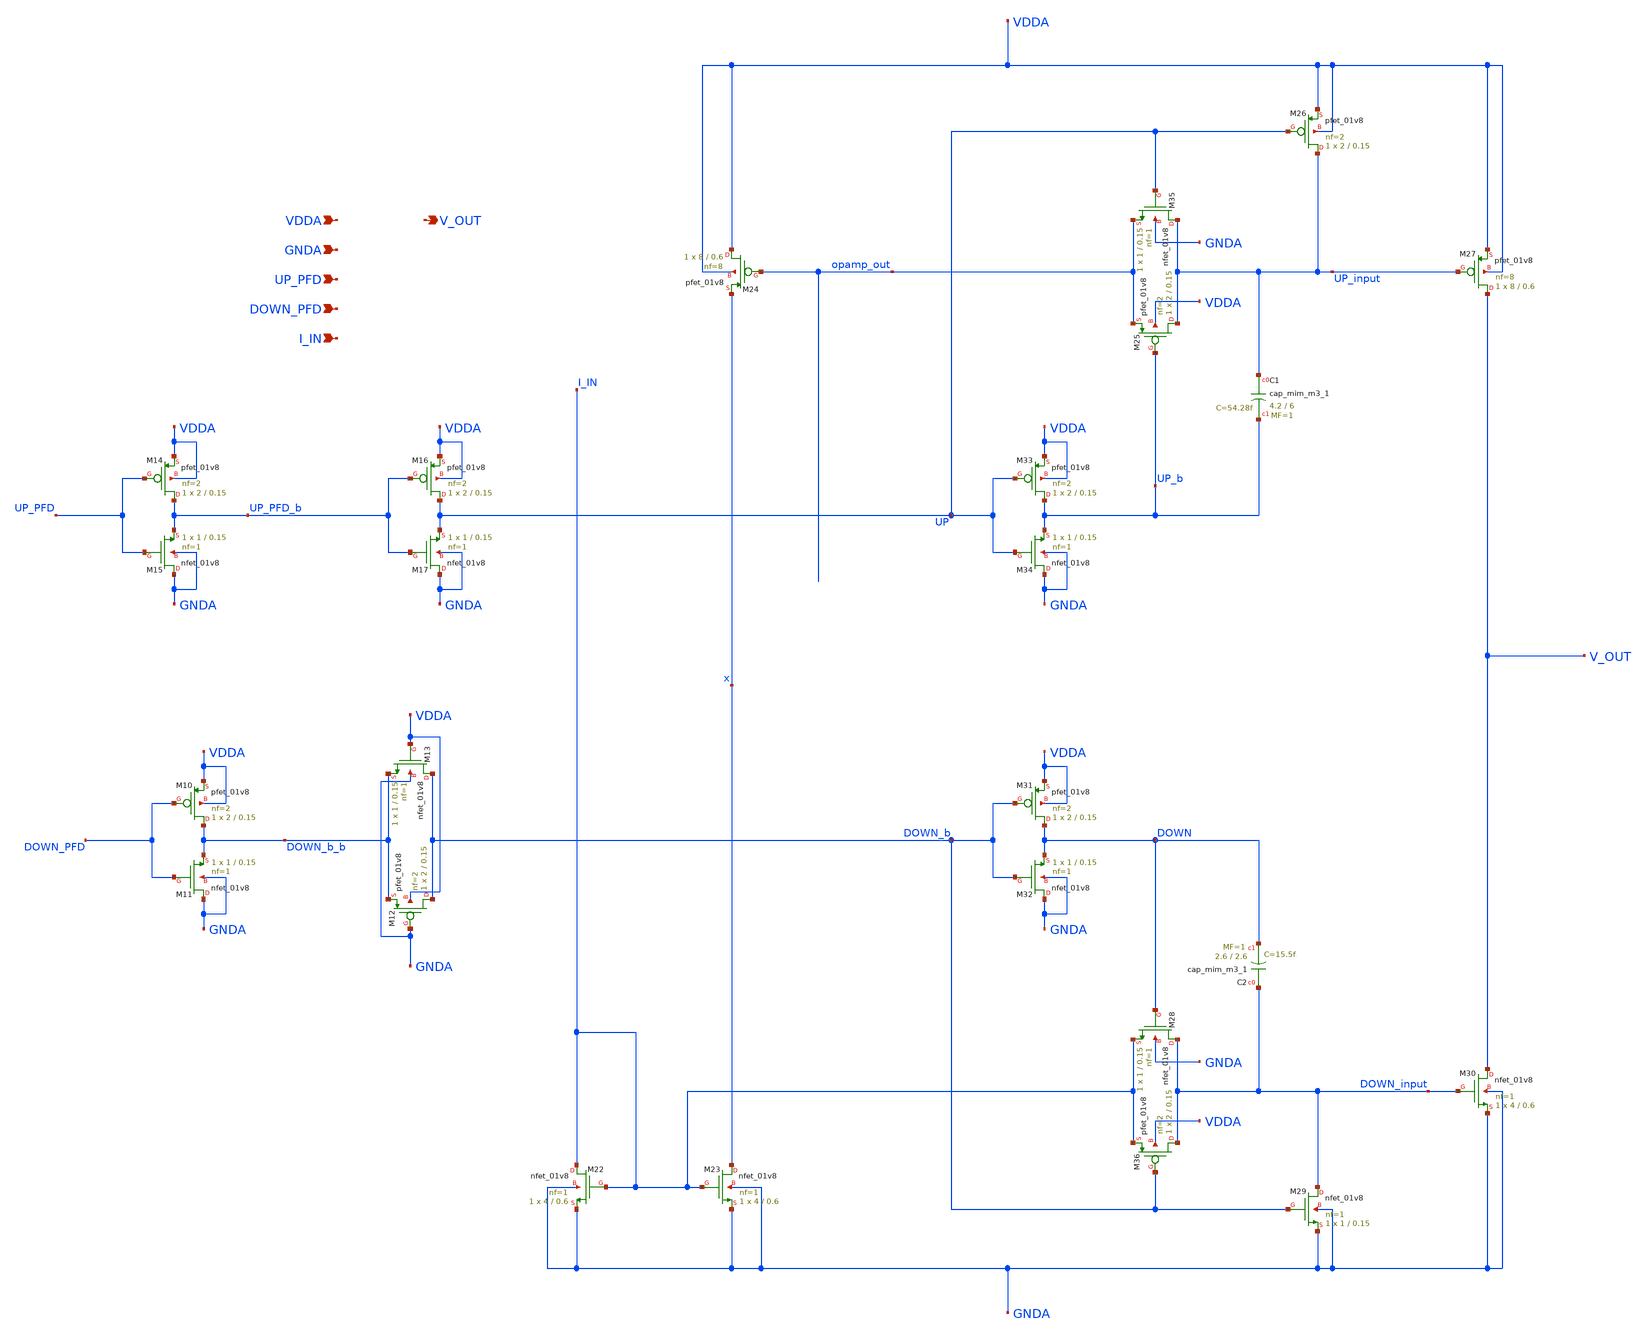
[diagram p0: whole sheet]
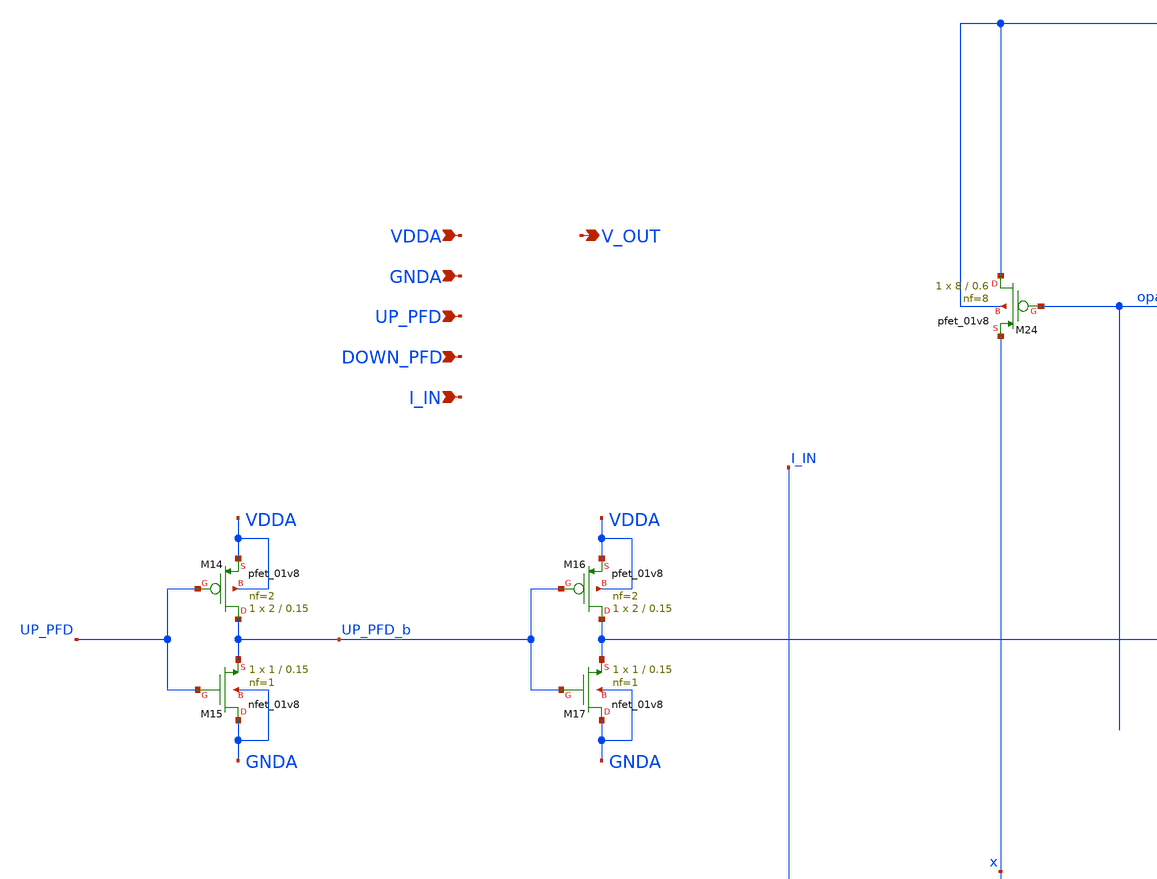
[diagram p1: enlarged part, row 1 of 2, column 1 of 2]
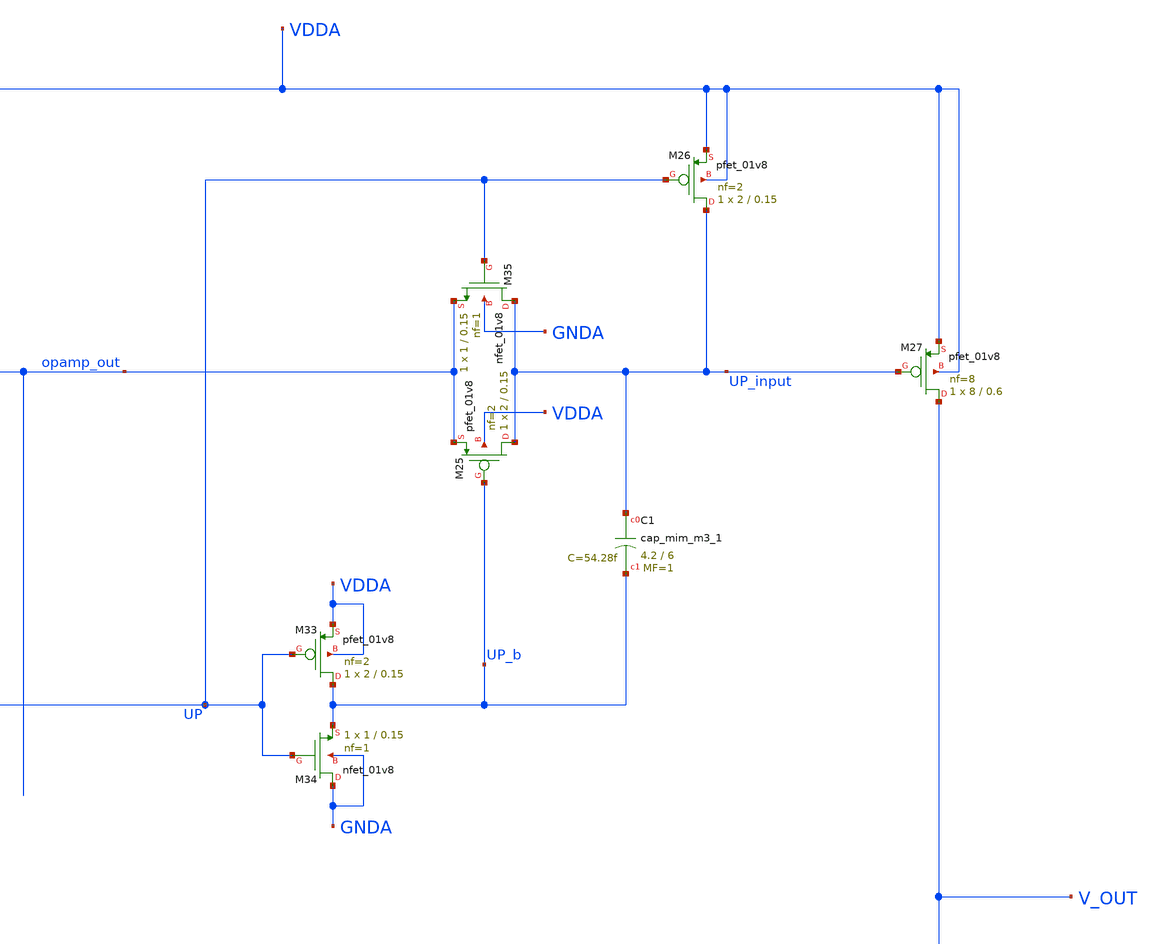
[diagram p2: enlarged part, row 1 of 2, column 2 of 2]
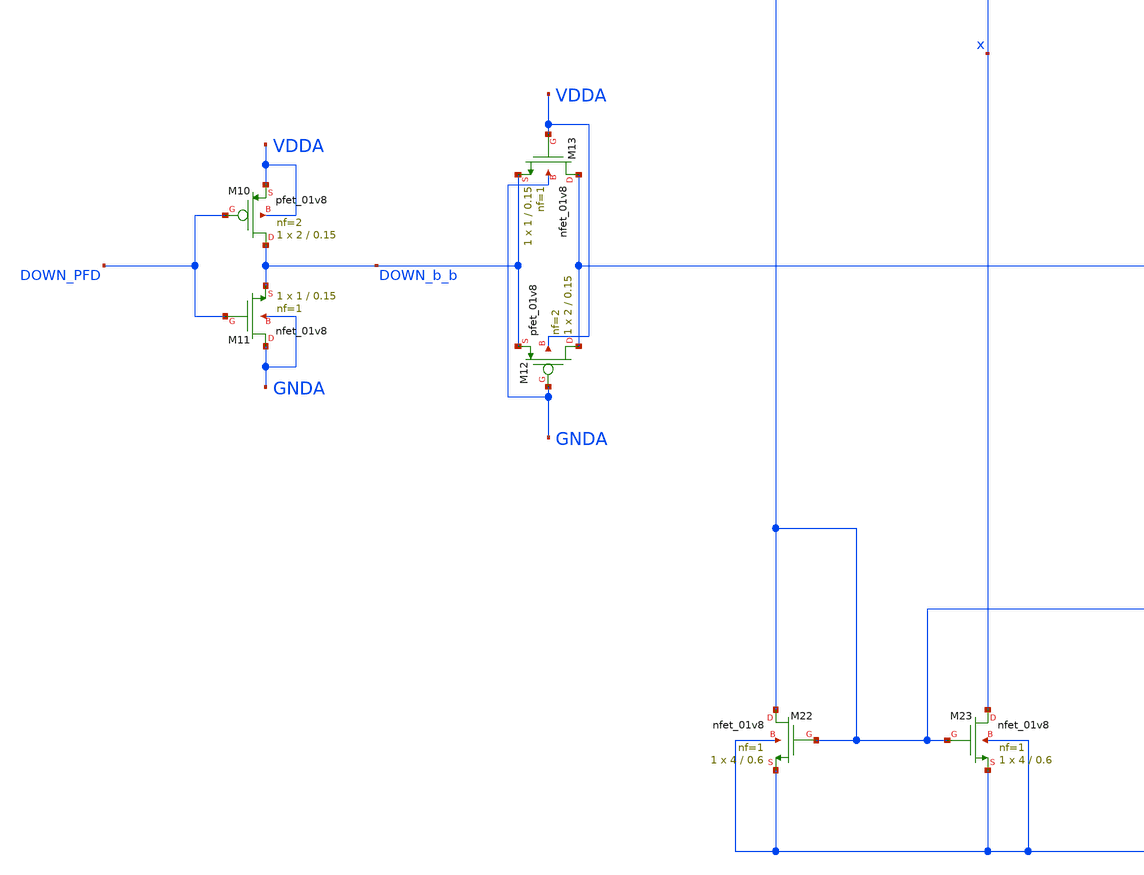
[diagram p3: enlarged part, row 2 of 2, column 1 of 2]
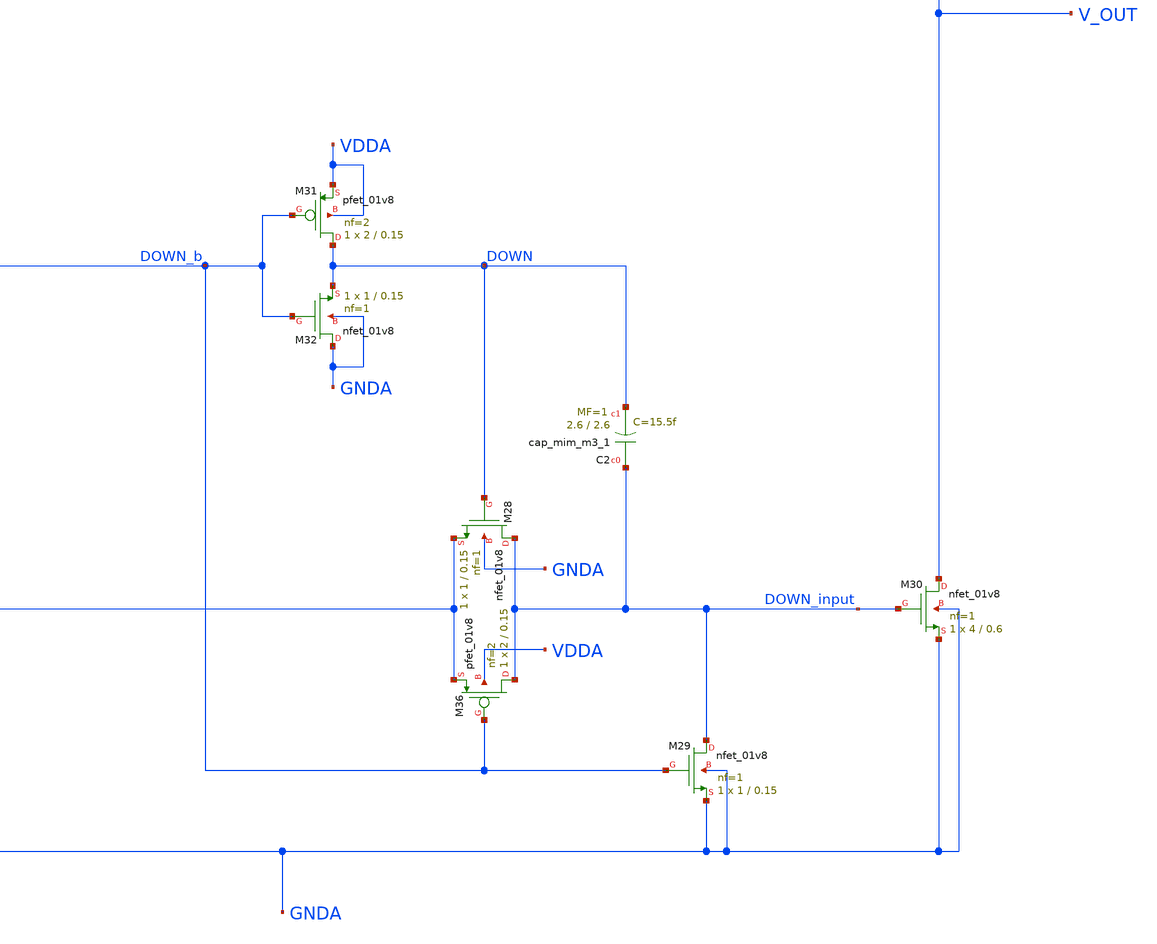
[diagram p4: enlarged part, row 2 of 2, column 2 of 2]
** sch_path: projects/pll/charge_pump/xschem_ngspice/charge_pump_xschem.sch
**.subckt charge_pump_xschem VDDA V_OUT GNDA UP_PFD DOWN_PFD I_IN
*.ipin VDDA
*.opin V_OUT
*.ipin GNDA
*.ipin UP_PFD
*.ipin DOWN_PFD
*.ipin I_IN
XM12 DOWN_b GNDA DOWN_b_b VDDA sky130_fd_pr__pfet_01v8 L=0.15 W=2 nf=2 ad='int((nf+1)/2) * W/nf * 0.29'
+ as='int((nf+2)/2) * W/nf * 0.29' pd='2*int((nf+1)/2) * (W/nf + 0.29)' ps='2*int((nf+2)/2) * (W/nf + 0.29)'
+ nrd='0.29 / W' nrs='0.29 / W' sa=0 sb=0 sd=0 mult=1 m=1
XM13 DOWN_b VDDA DOWN_b_b GNDA sky130_fd_pr__nfet_01v8 L=0.15 W=1 nf=1 ad='int((nf+1)/2) * W/nf * 0.29'
+ as='int((nf+2)/2) * W/nf * 0.29' pd='2*int((nf+1)/2) * (W/nf + 0.29)' ps='2*int((nf+2)/2) * (W/nf + 0.29)'
+ nrd='0.29 / W' nrs='0.29 / W' sa=0 sb=0 sd=0 mult=1 m=1
XM10 DOWN_b_b DOWN_PFD VDDA VDDA sky130_fd_pr__pfet_01v8 L=0.15 W=2 nf=2 ad='int((nf+1)/2) * W/nf * 0.29'
+ as='int((nf+2)/2) * W/nf * 0.29' pd='2*int((nf+1)/2) * (W/nf + 0.29)' ps='2*int((nf+2)/2) * (W/nf + 0.29)'
+ nrd='0.29 / W' nrs='0.29 / W' sa=0 sb=0 sd=0 mult=1 m=1
XM11 GNDA DOWN_PFD DOWN_b_b GNDA sky130_fd_pr__nfet_01v8 L=0.15 W=1 nf=1 ad='int((nf+1)/2) * W/nf * 0.29'
+ as='int((nf+2)/2) * W/nf * 0.29' pd='2*int((nf+1)/2) * (W/nf + 0.29)' ps='2*int((nf+2)/2) * (W/nf + 0.29)'
+ nrd='0.29 / W' nrs='0.29 / W' sa=0 sb=0 sd=0 mult=1 m=1
XM14 UP_PFD_b UP_PFD VDDA VDDA sky130_fd_pr__pfet_01v8 L=0.15 W=2 nf=2 ad='int((nf+1)/2) * W/nf * 0.29'
+ as='int((nf+2)/2) * W/nf * 0.29' pd='2*int((nf+1)/2) * (W/nf + 0.29)' ps='2*int((nf+2)/2) * (W/nf + 0.29)'
+ nrd='0.29 / W' nrs='0.29 / W' sa=0 sb=0 sd=0 mult=1 m=1
XM15 GNDA UP_PFD UP_PFD_b GNDA sky130_fd_pr__nfet_01v8 L=0.15 W=1 nf=1 ad='int((nf+1)/2) * W/nf * 0.29'
+ as='int((nf+2)/2) * W/nf * 0.29' pd='2*int((nf+1)/2) * (W/nf + 0.29)' ps='2*int((nf+2)/2) * (W/nf + 0.29)'
+ nrd='0.29 / W' nrs='0.29 / W' sa=0 sb=0 sd=0 mult=1 m=1
XM16 UP UP_PFD_b VDDA VDDA sky130_fd_pr__pfet_01v8 L=0.15 W=2 nf=2 ad='int((nf+1)/2) * W/nf * 0.29' as='int((nf+2)/2) * W/nf * 0.29'
+ pd='2*int((nf+1)/2) * (W/nf + 0.29)' ps='2*int((nf+2)/2) * (W/nf + 0.29)' nrd='0.29 / W' nrs='0.29 / W'
+ sa=0 sb=0 sd=0 mult=1 m=1
XM17 GNDA UP_PFD_b UP GNDA sky130_fd_pr__nfet_01v8 L=0.15 W=1 nf=1 ad='int((nf+1)/2) * W/nf * 0.29' as='int((nf+2)/2) * W/nf * 0.29'
+ pd='2*int((nf+1)/2) * (W/nf + 0.29)' ps='2*int((nf+2)/2) * (W/nf + 0.29)' nrd='0.29 / W' nrs='0.29 / W'
+ sa=0 sb=0 sd=0 mult=1 m=1
XM22 I_IN I_IN GNDA GNDA sky130_fd_pr__nfet_01v8 L=0.6 W=4 nf=1 ad='int((nf+1)/2) * W/nf * 0.29' as='int((nf+2)/2) * W/nf * 0.29'
+ pd='2*int((nf+1)/2) * (W/nf + 0.29)' ps='2*int((nf+2)/2) * (W/nf + 0.29)' nrd='0.29 / W' nrs='0.29 / W'
+ sa=0 sb=0 sd=0 mult=1 m=1
XM23 x I_IN GNDA GNDA sky130_fd_pr__nfet_01v8 L=0.6 W=4 nf=1 ad='int((nf+1)/2) * W/nf * 0.29' as='int((nf+2)/2) * W/nf * 0.29'
+ pd='2*int((nf+1)/2) * (W/nf + 0.29)' ps='2*int((nf+2)/2) * (W/nf + 0.29)' nrd='0.29 / W' nrs='0.29 / W'
+ sa=0 sb=0 sd=0 mult=1 m=1
XM24 VDDA opamp_out x VDDA sky130_fd_pr__pfet_01v8 L=0.6 W=8 nf=8 ad='int((nf+1)/2) * W/nf * 0.29' as='int((nf+2)/2) * W/nf * 0.29'
+ pd='2*int((nf+1)/2) * (W/nf + 0.29)' ps='2*int((nf+2)/2) * (W/nf + 0.29)' nrd='0.29 / W' nrs='0.29 / W'
+ sa=0 sb=0 sd=0 mult=1 m=1
XM25 UP_input UP_b opamp_out VDDA sky130_fd_pr__pfet_01v8 L=0.15 W=2 nf=2 ad='int((nf+1)/2) * W/nf * 0.29'
+ as='int((nf+2)/2) * W/nf * 0.29' pd='2*int((nf+1)/2) * (W/nf + 0.29)' ps='2*int((nf+2)/2) * (W/nf + 0.29)'
+ nrd='0.29 / W' nrs='0.29 / W' sa=0 sb=0 sd=0 mult=1 m=1
XM26 UP_input UP VDDA VDDA sky130_fd_pr__pfet_01v8 L=0.15 W=2 nf=2 ad='int((nf+1)/2) * W/nf * 0.29' as='int((nf+2)/2) * W/nf * 0.29'
+ pd='2*int((nf+1)/2) * (W/nf + 0.29)' ps='2*int((nf+2)/2) * (W/nf + 0.29)' nrd='0.29 / W' nrs='0.29 / W'
+ sa=0 sb=0 sd=0 mult=1 m=1
XM27 V_OUT UP_input VDDA VDDA sky130_fd_pr__pfet_01v8 L=0.6 W=8 nf=8 ad='int((nf+1)/2) * W/nf * 0.29'
+ as='int((nf+2)/2) * W/nf * 0.29' pd='2*int((nf+1)/2) * (W/nf + 0.29)' ps='2*int((nf+2)/2) * (W/nf + 0.29)'
+ nrd='0.29 / W' nrs='0.29 / W' sa=0 sb=0 sd=0 mult=1 m=1
XM28 DOWN_input DOWN I_IN GNDA sky130_fd_pr__nfet_01v8 L=0.15 W=1 nf=1 ad='int((nf+1)/2) * W/nf * 0.29'
+ as='int((nf+2)/2) * W/nf * 0.29' pd='2*int((nf+1)/2) * (W/nf + 0.29)' ps='2*int((nf+2)/2) * (W/nf + 0.29)'
+ nrd='0.29 / W' nrs='0.29 / W' sa=0 sb=0 sd=0 mult=1 m=1
XM29 DOWN_input DOWN_b GNDA GNDA sky130_fd_pr__nfet_01v8 L=0.15 W=1 nf=1 ad='int((nf+1)/2) * W/nf * 0.29'
+ as='int((nf+2)/2) * W/nf * 0.29' pd='2*int((nf+1)/2) * (W/nf + 0.29)' ps='2*int((nf+2)/2) * (W/nf + 0.29)'
+ nrd='0.29 / W' nrs='0.29 / W' sa=0 sb=0 sd=0 mult=1 m=1
XM30 V_OUT DOWN_input GNDA GNDA sky130_fd_pr__nfet_01v8 L=0.6 W=4 nf=1 ad='int((nf+1)/2) * W/nf * 0.29'
+ as='int((nf+2)/2) * W/nf * 0.29' pd='2*int((nf+1)/2) * (W/nf + 0.29)' ps='2*int((nf+2)/2) * (W/nf + 0.29)'
+ nrd='0.29 / W' nrs='0.29 / W' sa=0 sb=0 sd=0 mult=1 m=1
XM31 DOWN DOWN_b VDDA VDDA sky130_fd_pr__pfet_01v8 L=0.15 W=2 nf=2 ad='int((nf+1)/2) * W/nf * 0.29' as='int((nf+2)/2) * W/nf * 0.29'
+ pd='2*int((nf+1)/2) * (W/nf + 0.29)' ps='2*int((nf+2)/2) * (W/nf + 0.29)' nrd='0.29 / W' nrs='0.29 / W'
+ sa=0 sb=0 sd=0 mult=1 m=1
XM32 GNDA DOWN_b DOWN GNDA sky130_fd_pr__nfet_01v8 L=0.15 W=1 nf=1 ad='int((nf+1)/2) * W/nf * 0.29' as='int((nf+2)/2) * W/nf * 0.29'
+ pd='2*int((nf+1)/2) * (W/nf + 0.29)' ps='2*int((nf+2)/2) * (W/nf + 0.29)' nrd='0.29 / W' nrs='0.29 / W'
+ sa=0 sb=0 sd=0 mult=1 m=1
XM33 UP_b UP VDDA VDDA sky130_fd_pr__pfet_01v8 L=0.15 W=2 nf=2 ad='int((nf+1)/2) * W/nf * 0.29' as='int((nf+2)/2) * W/nf * 0.29'
+ pd='2*int((nf+1)/2) * (W/nf + 0.29)' ps='2*int((nf+2)/2) * (W/nf + 0.29)' nrd='0.29 / W' nrs='0.29 / W'
+ sa=0 sb=0 sd=0 mult=1 m=1
XM34 GNDA UP UP_b GNDA sky130_fd_pr__nfet_01v8 L=0.15 W=1 nf=1 ad='int((nf+1)/2) * W/nf * 0.29' as='int((nf+2)/2) * W/nf * 0.29'
+ pd='2*int((nf+1)/2) * (W/nf + 0.29)' ps='2*int((nf+2)/2) * (W/nf + 0.29)' nrd='0.29 / W' nrs='0.29 / W'
+ sa=0 sb=0 sd=0 mult=1 m=1
XM35 UP_input UP opamp_out GNDA sky130_fd_pr__nfet_01v8 L=0.15 W=1 nf=1 ad='int((nf+1)/2) * W/nf * 0.29'
+ as='int((nf+2)/2) * W/nf * 0.29' pd='2*int((nf+1)/2) * (W/nf + 0.29)' ps='2*int((nf+2)/2) * (W/nf + 0.29)'
+ nrd='0.29 / W' nrs='0.29 / W' sa=0 sb=0 sd=0 mult=1 m=1
XM36 DOWN_input DOWN_b I_IN VDDA sky130_fd_pr__pfet_01v8 L=0.15 W=2 nf=2 ad='int((nf+1)/2) * W/nf * 0.29'
+ as='int((nf+2)/2) * W/nf * 0.29' pd='2*int((nf+1)/2) * (W/nf + 0.29)' ps='2*int((nf+2)/2) * (W/nf + 0.29)'
+ nrd='0.29 / W' nrs='0.29 / W' sa=0 sb=0 sd=0 mult=1 m=1
XC1 UP_input UP_b sky130_fd_pr__cap_mim_m3_1 W=4.2 L=6 MF=1 m=1
XC2 DOWN_input DOWN sky130_fd_pr__cap_mim_m3_1 W=2.6 L=2.6 MF=1 m=1
**.ends
.end
